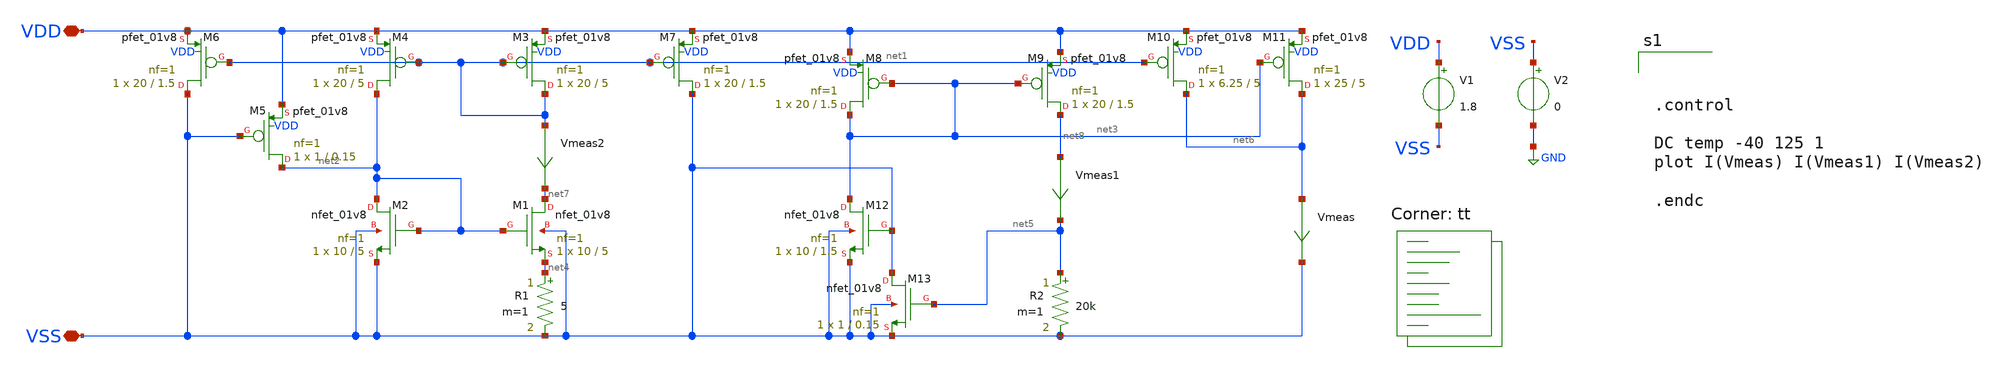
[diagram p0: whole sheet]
** sch_path: bandgap/current-ref/current-bandgap.sch
**.subckt current-bandgap VDD VSS
*.iopin VDD
*.iopin VSS
XM1 net7 net2 net4 VSS sky130_fd_pr__nfet_01v8 L=5 W=10 nf=1 ad='int((nf+1)/2) * W/nf * 0.29' as='int((nf+2)/2) * W/nf * 0.29'
+ pd='2*int((nf+1)/2) * (W/nf + 0.29)' ps='2*int((nf+2)/2) * (W/nf + 0.29)' nrd='0.29 / W' nrs='0.29 / W'
+ sa=0 sb=0 sd=0 mult=1 m=1
XM2 net2 net2 VSS VSS sky130_fd_pr__nfet_01v8 L=5 W=10 nf=1 ad='int((nf+1)/2) * W/nf * 0.29' as='int((nf+2)/2) * W/nf * 0.29'
+ pd='2*int((nf+1)/2) * (W/nf + 0.29)' ps='2*int((nf+2)/2) * (W/nf + 0.29)' nrd='0.29 / W' nrs='0.29 / W'
+ sa=0 sb=0 sd=0 mult=1 m=1
XM3 net1 net1 VDD VDD sky130_fd_pr__pfet_01v8 L=5 W=20 nf=1 ad='int((nf+1)/2) * W/nf * 0.29' as='int((nf+2)/2) * W/nf * 0.29'
+ pd='2*int((nf+1)/2) * (W/nf + 0.29)' ps='2*int((nf+2)/2) * (W/nf + 0.29)' nrd='0.29 / W' nrs='0.29 / W'
+ sa=0 sb=0 sd=0 mult=1 m=1
XM4 net2 net1 VDD VDD sky130_fd_pr__pfet_01v8 L=5 W=20 nf=1 ad='int((nf+1)/2) * W/nf * 0.29' as='int((nf+2)/2) * W/nf * 0.29'
+ pd='2*int((nf+1)/2) * (W/nf + 0.29)' ps='2*int((nf+2)/2) * (W/nf + 0.29)' nrd='0.29 / W' nrs='0.29 / W'
+ sa=0 sb=0 sd=0 mult=1 m=1
XM5 net2 VSS VDD VDD sky130_fd_pr__pfet_01v8 L=0.15 W=1 nf=1 ad='int((nf+1)/2) * W/nf * 0.29' as='int((nf+2)/2) * W/nf * 0.29'
+ pd='2*int((nf+1)/2) * (W/nf + 0.29)' ps='2*int((nf+2)/2) * (W/nf + 0.29)' nrd='0.29 / W' nrs='0.29 / W'
+ sa=0 sb=0 sd=0 mult=1 m=1
XM6 VSS net1 VDD VDD sky130_fd_pr__pfet_01v8 L=1.5 W=20 nf=1 ad='int((nf+1)/2) * W/nf * 0.29' as='int((nf+2)/2) * W/nf * 0.29'
+ pd='2*int((nf+1)/2) * (W/nf + 0.29)' ps='2*int((nf+2)/2) * (W/nf + 0.29)' nrd='0.29 / W' nrs='0.29 / W'
+ sa=0 sb=0 sd=0 mult=1 m=1
XM7 VSS net1 VDD VDD sky130_fd_pr__pfet_01v8 L=1.5 W=20 nf=1 ad='int((nf+1)/2) * W/nf * 0.29' as='int((nf+2)/2) * W/nf * 0.29'
+ pd='2*int((nf+1)/2) * (W/nf + 0.29)' ps='2*int((nf+2)/2) * (W/nf + 0.29)' nrd='0.29 / W' nrs='0.29 / W'
+ sa=0 sb=0 sd=0 mult=1 m=1
XM8 net3 net3 VDD VDD sky130_fd_pr__pfet_01v8 L=1.5 W=20 nf=1 ad='int((nf+1)/2) * W/nf * 0.29' as='int((nf+2)/2) * W/nf * 0.29'
+ pd='2*int((nf+1)/2) * (W/nf + 0.29)' ps='2*int((nf+2)/2) * (W/nf + 0.29)' nrd='0.29 / W' nrs='0.29 / W'
+ sa=0 sb=0 sd=0 mult=1 m=1
XM9 net8 net3 VDD VDD sky130_fd_pr__pfet_01v8 L=1.5 W=20 nf=1 ad='int((nf+1)/2) * W/nf * 0.29' as='int((nf+2)/2) * W/nf * 0.29'
+ pd='2*int((nf+1)/2) * (W/nf + 0.29)' ps='2*int((nf+2)/2) * (W/nf + 0.29)' nrd='0.29 / W' nrs='0.29 / W'
+ sa=0 sb=0 sd=0 mult=1 m=1
XM10 net6 net1 VDD VDD sky130_fd_pr__pfet_01v8 L=5 W=6.25 nf=1 ad='int((nf+1)/2) * W/nf * 0.29' as='int((nf+2)/2) * W/nf * 0.29'
+ pd='2*int((nf+1)/2) * (W/nf + 0.29)' ps='2*int((nf+2)/2) * (W/nf + 0.29)' nrd='0.29 / W' nrs='0.29 / W'
+ sa=0 sb=0 sd=0 mult=1 m=1
XM11 net6 net3 VDD VDD sky130_fd_pr__pfet_01v8 L=5 W=25 nf=1 ad='int((nf+1)/2) * W/nf * 0.29' as='int((nf+2)/2) * W/nf * 0.29'
+ pd='2*int((nf+1)/2) * (W/nf + 0.29)' ps='2*int((nf+2)/2) * (W/nf + 0.29)' nrd='0.29 / W' nrs='0.29 / W'
+ sa=0 sb=0 sd=0 mult=1 m=1
XM12 net3 VSS VSS VSS sky130_fd_pr__nfet_01v8 L=1.5 W=10 nf=1 ad='int((nf+1)/2) * W/nf * 0.29' as='int((nf+2)/2) * W/nf * 0.29'
+ pd='2*int((nf+1)/2) * (W/nf + 0.29)' ps='2*int((nf+2)/2) * (W/nf + 0.29)' nrd='0.29 / W' nrs='0.29 / W'
+ sa=0 sb=0 sd=0 mult=1 m=1
XM13 VSS net5 VSS VSS sky130_fd_pr__nfet_01v8 L=0.15 W=1 nf=1 ad='int((nf+1)/2) * W/nf * 0.29' as='int((nf+2)/2) * W/nf * 0.29'
+ pd='2*int((nf+1)/2) * (W/nf + 0.29)' ps='2*int((nf+2)/2) * (W/nf + 0.29)' nrd='0.29 / W' nrs='0.29 / W'
+ sa=0 sb=0 sd=0 mult=1 m=1
R1 net4 VSS 5 m=1
R2 net5 VSS 20k m=1
V1 VDD VSS 1.8
V2 VSS GND 0
Vmeas net6 VSS 0
.save i(vmeas)
Vmeas1 net8 net5 0
.save i(vmeas1)
Vmeas2 net1 net7 0
.save i(vmeas2)
**** begin user architecture code
.lib $::SKYWATER_MODELS/sky130.lib.spice tt



.control

DC temp -40 125 1
plot I(Vmeas) I(Vmeas1) I(Vmeas2)

.endc


**** end user architecture code
**.ends
.GLOBAL GND
.end
